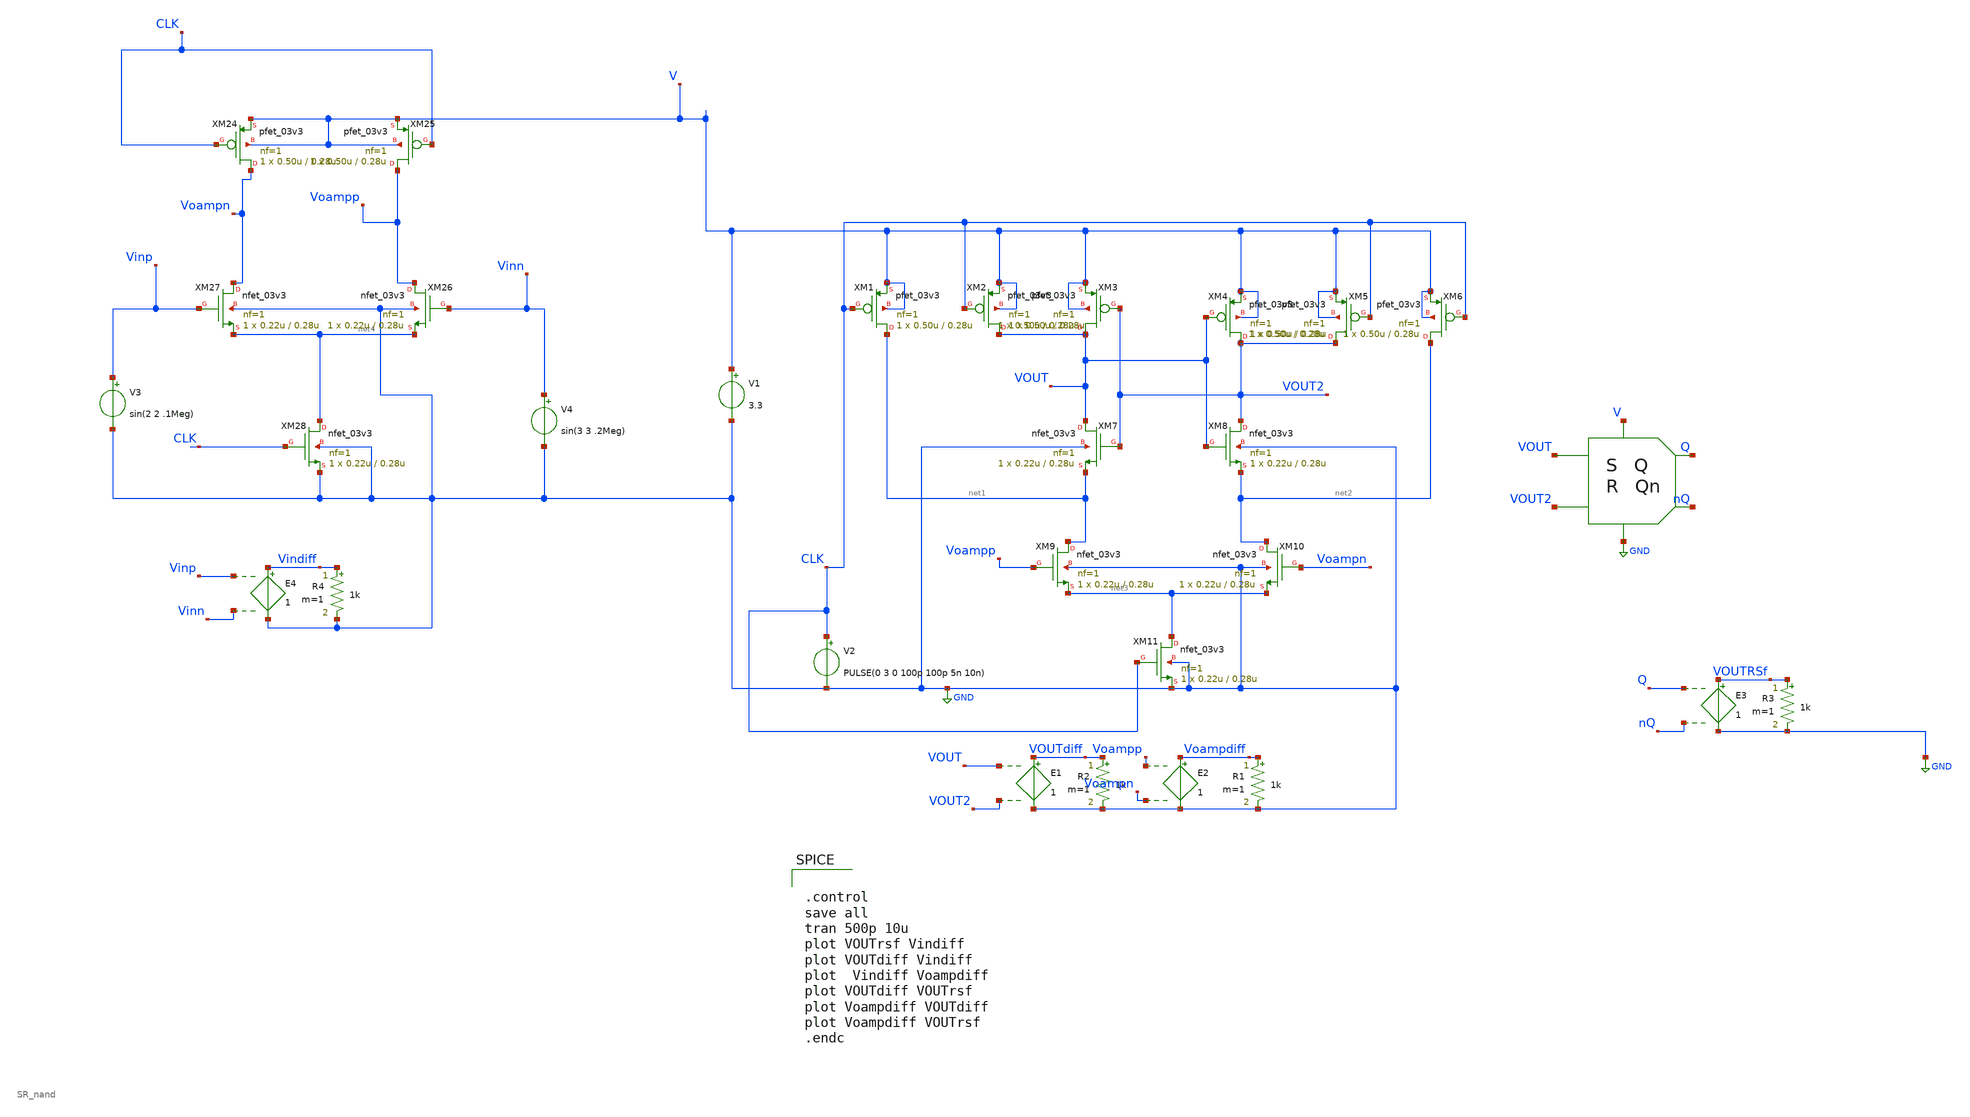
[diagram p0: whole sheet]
** sch_path: Comparador_pream_Slatch.sch
**.subckt Comparador_pream_Slatch
XM1 net1 CLK V V pfet_03v3 L=0.28u W=0.50u nf=1 ad='int((nf+1)/2) * W/nf * 0.18u' as='int((nf+2)/2) * W/nf * 0.18u'
+ pd='2*int((nf+1)/2) * (W/nf + 0.18u)' ps='2*int((nf+2)/2) * (W/nf + 0.18u)' nrd='0.18u / W' nrs='0.18u / W'
+ sa=0 sb=0 sd=0 m=1
XM2 VOUT CLK V V pfet_03v3 L=0.28u W=0.50u nf=1 ad='int((nf+1)/2) * W/nf * 0.18u' as='int((nf+2)/2) * W/nf * 0.18u'
+ pd='2*int((nf+1)/2) * (W/nf + 0.18u)' ps='2*int((nf+2)/2) * (W/nf + 0.18u)' nrd='0.18u / W' nrs='0.18u / W'
+ sa=0 sb=0 sd=0 m=1
XM3 VOUT VOUT2 V V pfet_03v3 L=0.28u W=0.50u nf=1 ad='int((nf+1)/2) * W/nf * 0.18u' as='int((nf+2)/2) * W/nf * 0.18u'
+ pd='2*int((nf+1)/2) * (W/nf + 0.18u)' ps='2*int((nf+2)/2) * (W/nf + 0.18u)' nrd='0.18u / W' nrs='0.18u / W'
+ sa=0 sb=0 sd=0 m=1
XM4 VOUT2 VOUT V V pfet_03v3 L=0.28u W=0.50u nf=1 ad='int((nf+1)/2) * W/nf * 0.18u' as='int((nf+2)/2) * W/nf * 0.18u'
+ pd='2*int((nf+1)/2) * (W/nf + 0.18u)' ps='2*int((nf+2)/2) * (W/nf + 0.18u)' nrd='0.18u / W' nrs='0.18u / W'
+ sa=0 sb=0 sd=0 m=1
XM5 VOUT2 CLK V V pfet_03v3 L=0.28u W=0.50u nf=1 ad='int((nf+1)/2) * W/nf * 0.18u' as='int((nf+2)/2) * W/nf * 0.18u'
+ pd='2*int((nf+1)/2) * (W/nf + 0.18u)' ps='2*int((nf+2)/2) * (W/nf + 0.18u)' nrd='0.18u / W' nrs='0.18u / W'
+ sa=0 sb=0 sd=0 m=1
XM6 net2 CLK V V pfet_03v3 L=0.28u W=0.50u nf=1 ad='int((nf+1)/2) * W/nf * 0.18u' as='int((nf+2)/2) * W/nf * 0.18u'
+ pd='2*int((nf+1)/2) * (W/nf + 0.18u)' ps='2*int((nf+2)/2) * (W/nf + 0.18u)' nrd='0.18u / W' nrs='0.18u / W'
+ sa=0 sb=0 sd=0 m=1
XM7 VOUT VOUT2 net1 GND nfet_03v3 L=0.28u W=0.22u nf=1 ad='int((nf+1)/2) * W/nf * 0.18u' as='int((nf+2)/2) * W/nf * 0.18u'
+ pd='2*int((nf+1)/2) * (W/nf + 0.18u)' ps='2*int((nf+2)/2) * (W/nf + 0.18u)' nrd='0.18u / W' nrs='0.18u / W'
+ sa=0 sb=0 sd=0 m=1
XM8 VOUT2 VOUT net2 GND nfet_03v3 L=0.28u W=0.22u nf=1 ad='int((nf+1)/2) * W/nf * 0.18u' as='int((nf+2)/2) * W/nf * 0.18u'
+ pd='2*int((nf+1)/2) * (W/nf + 0.18u)' ps='2*int((nf+2)/2) * (W/nf + 0.18u)' nrd='0.18u / W' nrs='0.18u / W'
+ sa=0 sb=0 sd=0 m=1
XM9 net1 Voampp net3 GND nfet_03v3 L=0.28u W=0.22u nf=1 ad='int((nf+1)/2) * W/nf * 0.18u' as='int((nf+2)/2) * W/nf * 0.18u'
+ pd='2*int((nf+1)/2) * (W/nf + 0.18u)' ps='2*int((nf+2)/2) * (W/nf + 0.18u)' nrd='0.18u / W' nrs='0.18u / W'
+ sa=0 sb=0 sd=0 m=1
XM10 net2 Voampn net3 GND nfet_03v3 L=0.28u W=0.22u nf=1 ad='int((nf+1)/2) * W/nf * 0.18u' as='int((nf+2)/2) * W/nf * 0.18u'
+ pd='2*int((nf+1)/2) * (W/nf + 0.18u)' ps='2*int((nf+2)/2) * (W/nf + 0.18u)' nrd='0.18u / W' nrs='0.18u / W'
+ sa=0 sb=0 sd=0 m=1
XM11 net3 CLK GND GND nfet_03v3 L=0.28u W=0.22u nf=1 ad='int((nf+1)/2) * W/nf * 0.18u' as='int((nf+2)/2) * W/nf * 0.18u'
+ pd='2*int((nf+1)/2) * (W/nf + 0.18u)' ps='2*int((nf+2)/2) * (W/nf + 0.18u)' nrd='0.18u / W' nrs='0.18u / W'
+ sa=0 sb=0 sd=0 m=1
V1 V GND 3.3
V2 CLK GND PULSE(0 3 0 100p 100p 5n 10n)
R2 VOUTdiff GND 1k m=1
E1 VOUTdiff GND VOUT VOUT2 1
R1 Voampdiff GND 1k m=1
E2 Voampdiff GND Voampp Voampn 1
R3 VOUTRSf GND 1k m=1
E3 VOUTRSf GND Q nQ 1
XM26 Voampp Vinn net4 GND nfet_03v3 L=0.28u W=0.22u nf=1 ad='int((nf+1)/2) * W/nf * 0.18u' as='int((nf+2)/2) * W/nf * 0.18u'
+ pd='2*int((nf+1)/2) * (W/nf + 0.18u)' ps='2*int((nf+2)/2) * (W/nf + 0.18u)' nrd='0.18u / W' nrs='0.18u / W'
+ sa=0 sb=0 sd=0 m=1
XM27 Voampn Vinp net4 GND nfet_03v3 L=0.28u W=0.22u nf=1 ad='int((nf+1)/2) * W/nf * 0.18u' as='int((nf+2)/2) * W/nf * 0.18u'
+ pd='2*int((nf+1)/2) * (W/nf + 0.18u)' ps='2*int((nf+2)/2) * (W/nf + 0.18u)' nrd='0.18u / W' nrs='0.18u / W'
+ sa=0 sb=0 sd=0 m=1
V3 Vinp GND sin(2 2 .1Meg)
V4 Vinn GND sin(3 3 .2Meg)
R4 Vindiff GND 1k m=1
E4 Vindiff GND Vinp Vinn 1
XM28 net4 CLK GND GND nfet_03v3 L=0.28u W=0.22u nf=1 ad='int((nf+1)/2) * W/nf * 0.18u' as='int((nf+2)/2) * W/nf * 0.18u'
+ pd='2*int((nf+1)/2) * (W/nf + 0.18u)' ps='2*int((nf+2)/2) * (W/nf + 0.18u)' nrd='0.18u / W' nrs='0.18u / W'
+ sa=0 sb=0 sd=0 m=1
XM24 Voampn CLK V V pfet_03v3 L=0.28u W=0.50u nf=1 ad='int((nf+1)/2) * W/nf * 0.18u' as='int((nf+2)/2) * W/nf * 0.18u'
+ pd='2*int((nf+1)/2) * (W/nf + 0.18u)' ps='2*int((nf+2)/2) * (W/nf + 0.18u)' nrd='0.18u / W' nrs='0.18u / W'
+ sa=0 sb=0 sd=0 m=1
XM25 Voampp CLK V V pfet_03v3 L=0.28u W=0.50u nf=1 ad='int((nf+1)/2) * W/nf * 0.18u' as='int((nf+2)/2) * W/nf * 0.18u'
+ pd='2*int((nf+1)/2) * (W/nf + 0.18u)' ps='2*int((nf+2)/2) * (W/nf + 0.18u)' nrd='0.18u / W' nrs='0.18u / W'
+ sa=0 sb=0 sd=0 m=1
X1 VOUT V GND VOUT2 Q nQ SR_nand
**** begin user architecture code


.control
save all
tran 500p 10u
plot VOUTrsf Vindiff
plot VOUTdiff Vindiff
plot  Vindiff Voampdiff
plot VOUTdiff VOUTrsf
plot Voampdiff VOUTdiff
plot Voampdiff VOUTrsf
.endc


.include /foss/pdks/gf180mcuC/libs.tech/ngspice/design.ngspice
.lib /foss/pdks/gf180mcuC/libs.tech/ngspice/sm141064.ngspice typical

**** end user architecture code
**.ends

* expanding   symbol:  jesusu/Simbolos/SR_nand.sym # of pins=6
** sym_path: Simbolos/SR_nand.sym
** sch_path: Simbolos/SR_nand.sch
.subckt SR_nand S V GND R Q Qn
*.iopin S
*.iopin R
*.iopin V
*.iopin GND
*.iopin Qn
*.iopin Q
XM1 Qn S V V pfet_03v3 L=0.28u W=4u nf=1 ad='int((nf+1)/2) * W/nf * 0.18u' as='int((nf+2)/2) * W/nf * 0.18u'
+ pd='2*int((nf+1)/2) * (W/nf + 0.18u)' ps='2*int((nf+2)/2) * (W/nf + 0.18u)' nrd='0.18u / W' nrs='0.18u / W'
+ sa=0 sb=0 sd=0 m=1
XM2 Qn Q net1 GND nfet_03v3 L=0.28u W=4u nf=1 ad='int((nf+1)/2) * W/nf * 0.18u' as='int((nf+2)/2) * W/nf * 0.18u'
+ pd='2*int((nf+1)/2) * (W/nf + 0.18u)' ps='2*int((nf+2)/2) * (W/nf + 0.18u)' nrd='0.18u / W' nrs='0.18u / W'
+ sa=0 sb=0 sd=0 m=1
XM3 Q Qn V V pfet_03v3 L=0.28u W=4u nf=1 ad='int((nf+1)/2) * W/nf * 0.18u' as='int((nf+2)/2) * W/nf * 0.18u'
+ pd='2*int((nf+1)/2) * (W/nf + 0.18u)' ps='2*int((nf+2)/2) * (W/nf + 0.18u)' nrd='0.18u / W' nrs='0.18u / W'
+ sa=0 sb=0 sd=0 m=1
XM4 Q R V V pfet_03v3 L=0.28u W=4u nf=1 ad='int((nf+1)/2) * W/nf * 0.18u' as='int((nf+2)/2) * W/nf * 0.18u'
+ pd='2*int((nf+1)/2) * (W/nf + 0.18u)' ps='2*int((nf+2)/2) * (W/nf + 0.18u)' nrd='0.18u / W' nrs='0.18u / W'
+ sa=0 sb=0 sd=0 m=1
XM5 Qn Q V V pfet_03v3 L=0.28u W=4u nf=1 ad='int((nf+1)/2) * W/nf * 0.18u' as='int((nf+2)/2) * W/nf * 0.18u'
+ pd='2*int((nf+1)/2) * (W/nf + 0.18u)' ps='2*int((nf+2)/2) * (W/nf + 0.18u)' nrd='0.18u / W' nrs='0.18u / W'
+ sa=0 sb=0 sd=0 m=1
XM6 net1 S GND GND nfet_03v3 L=0.28u W=4u nf=1 ad='int((nf+1)/2) * W/nf * 0.18u' as='int((nf+2)/2) * W/nf * 0.18u'
+ pd='2*int((nf+1)/2) * (W/nf + 0.18u)' ps='2*int((nf+2)/2) * (W/nf + 0.18u)' nrd='0.18u / W' nrs='0.18u / W'
+ sa=0 sb=0 sd=0 m=1
XM7 Q Qn net2 GND nfet_03v3 L=0.28u W=4u nf=1 ad='int((nf+1)/2) * W/nf * 0.18u' as='int((nf+2)/2) * W/nf * 0.18u'
+ pd='2*int((nf+1)/2) * (W/nf + 0.18u)' ps='2*int((nf+2)/2) * (W/nf + 0.18u)' nrd='0.18u / W' nrs='0.18u / W'
+ sa=0 sb=0 sd=0 m=1
XM8 net2 R GND GND nfet_03v3 L=0.28u W=2u nf=1 ad='int((nf+1)/2) * W/nf * 0.18u' as='int((nf+2)/2) * W/nf * 0.18u'
+ pd='2*int((nf+1)/2) * (W/nf + 0.18u)' ps='2*int((nf+2)/2) * (W/nf + 0.18u)' nrd='0.18u / W' nrs='0.18u / W'
+ sa=0 sb=0 sd=0 m=1
.ends

.GLOBAL GND
.end
